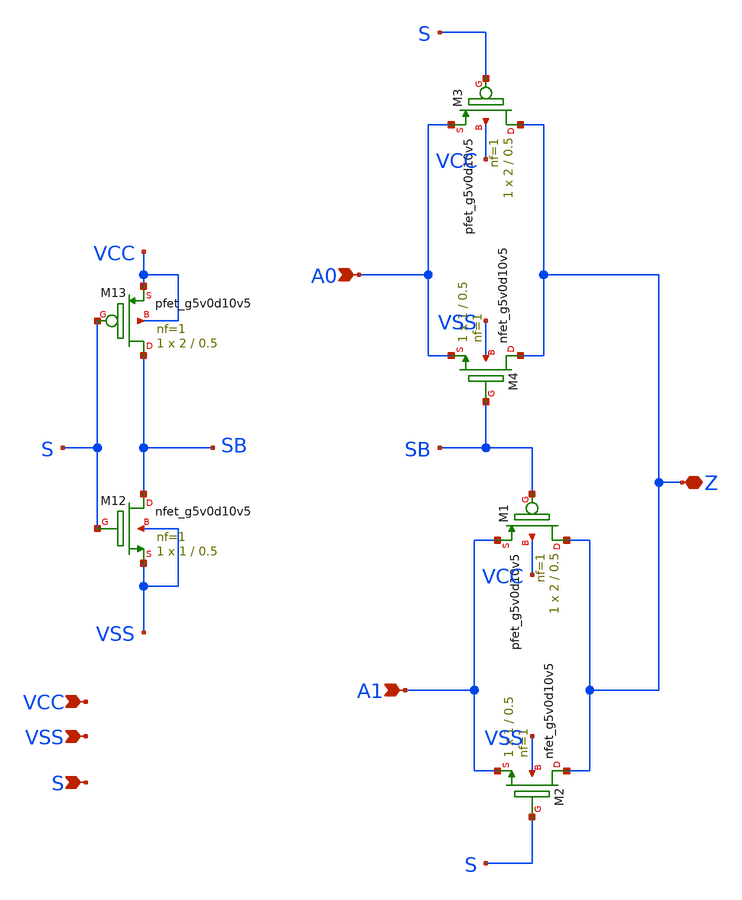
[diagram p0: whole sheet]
** sch_path: xschem_lvs/mux2to1.sch
**.subckt mux2to1 VCC VSS A0 A1 Z S
*.ipin VCC
*.ipin VSS
*.ipin A0
*.ipin A1
*.iopin Z
*.ipin S
XM12 SB S VSS VSS sky130_fd_pr__nfet_g5v0d10v5 L=0.5 W=1 nf=1 ad='int((nf+1)/2) * W/nf * 0.29' as='int((nf+2)/2) * W/nf * 0.29'
+ pd='2*int((nf+1)/2) * (W/nf + 0.29)' ps='2*int((nf+2)/2) * (W/nf + 0.29)' nrd='0.29 / W' nrs='0.29 / W'
+ sa=0 sb=0 sd=0 mult=1 m=1
XM13 SB S VCC VCC sky130_fd_pr__pfet_g5v0d10v5 L=0.5 W=2 nf=1 ad='int((nf+1)/2) * W/nf * 0.29' as='int((nf+2)/2) * W/nf * 0.29'
+ pd='2*int((nf+1)/2) * (W/nf + 0.29)' ps='2*int((nf+2)/2) * (W/nf + 0.29)' nrd='0.29 / W' nrs='0.29 / W'
+ sa=0 sb=0 sd=0 mult=1 m=1
XM3 Z S A0 VCC sky130_fd_pr__pfet_g5v0d10v5 L=0.5 W=2 nf=1 ad='int((nf+1)/2) * W/nf * 0.29' as='int((nf+2)/2) * W/nf * 0.29'
+ pd='2*int((nf+1)/2) * (W/nf + 0.29)' ps='2*int((nf+2)/2) * (W/nf + 0.29)' nrd='0.29 / W' nrs='0.29 / W'
+ sa=0 sb=0 sd=0 mult=1 m=1
XM4 Z SB A0 VSS sky130_fd_pr__nfet_g5v0d10v5 L=0.5 W=1 nf=1 ad='int((nf+1)/2) * W/nf * 0.29' as='int((nf+2)/2) * W/nf * 0.29'
+ pd='2*int((nf+1)/2) * (W/nf + 0.29)' ps='2*int((nf+2)/2) * (W/nf + 0.29)' nrd='0.29 / W' nrs='0.29 / W'
+ sa=0 sb=0 sd=0 mult=1 m=1
XM1 Z SB A1 VCC sky130_fd_pr__pfet_g5v0d10v5 L=0.5 W=2 nf=1 ad='int((nf+1)/2) * W/nf * 0.29' as='int((nf+2)/2) * W/nf * 0.29'
+ pd='2*int((nf+1)/2) * (W/nf + 0.29)' ps='2*int((nf+2)/2) * (W/nf + 0.29)' nrd='0.29 / W' nrs='0.29 / W'
+ sa=0 sb=0 sd=0 mult=1 m=1
XM2 Z S A1 VSS sky130_fd_pr__nfet_g5v0d10v5 L=0.5 W=1 nf=1 ad='int((nf+1)/2) * W/nf * 0.29' as='int((nf+2)/2) * W/nf * 0.29'
+ pd='2*int((nf+1)/2) * (W/nf + 0.29)' ps='2*int((nf+2)/2) * (W/nf + 0.29)' nrd='0.29 / W' nrs='0.29 / W'
+ sa=0 sb=0 sd=0 mult=1 m=1
**.ends
.end
